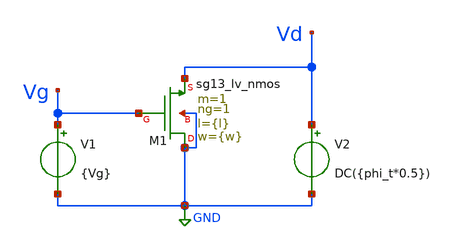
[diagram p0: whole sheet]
** sch_path: Parametros_Psp/VTH_test.sch
**.subckt VTH_test
V1 Vg GND {Vg}
V2 Vd GND DC({phi_t*0.5})
XM1 GND Vg Vd GND sg13_lv_nmos w={w} l={l} ng=1 m=1 mm_ok=1
**** begin user architecture code


* Circuit Parameters
.param vg = 3
.param step = 0.01
.param phi_t = 0.0258
.param w = 5.0u
.param l = 0.18u
* Include Models
.lib /opt/pdks/ihp-sg13g2/libs.tech/ngspice/models/cornerMOSlv.lib mos_tt
.lib /opt/pdks/ihp-sg13g2/libs.tech/ngspice/models/cornerMOShv.lib mos_tt
* OP Parameters & Singals to save
.save all
*Simulations
.dc V1 0 {vg} {step}
.control
run
setplot dc1
plot -i(V2)
set filetype = ascii
write dcsweep.raw
.endc
.end


**** end user architecture code
**.ends
.GLOBAL GND
.end
